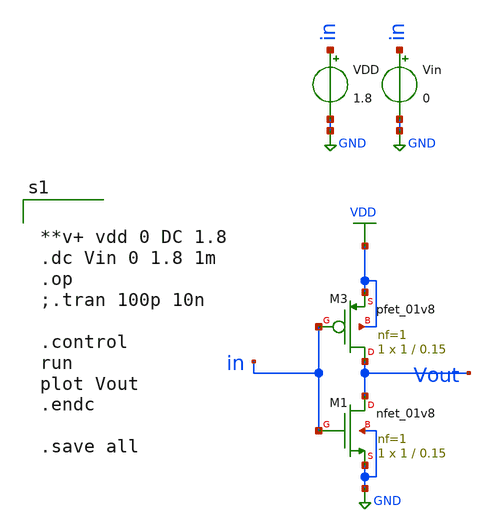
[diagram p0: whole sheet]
** sch_path: inverter.sch
**.subckt inverter
XM3 Vout in VDD VDD sky130_fd_pr__pfet_01v8 L=0.15 W=1 nf=1 ad='int((1 + 1)/2) * 1 / 1 * 0.29' as='int((1 + 2)/2) * 1 / 1 * 0.29'
+ pd='2*int((1 + 1)/2) * (1 / 1 + 0.29)' ps='2*int((1 + 2)/2) * (1 / 1 + 0.29)' nrd='0.29 / 1 ' nrs='0.29 / 1 '
+ sa=0 sb=0 sd=0 mult=1 m=1
Vin in GND 0
XM1 Vout in GND GND sky130_fd_pr__nfet_01v8 L=0.15 W=1 nf=1 ad='int((1 + 1)/2) * 1 / 1 * 0.29' as='int((1 + 2)/2) * 1 / 1 * 0.29'
+ pd='2*int((1 + 1)/2) * (1 / 1 + 0.29)' ps='2*int((1 + 2)/2) * (1 / 1 + 0.29)' nrd='0.29 / 1 ' nrs='0.29 / 1 '
+ sa=0 sb=0 sd=0 mult=1 m=1
VDD in GND 1.8
**** begin user architecture code


**v+ vdd 0 DC 1.8
.dc Vin 0 1.8 1m
.op
;.tran 100p 10n

.control
run
plot Vout
.endc

.save all


**** end user architecture code
**.ends
.GLOBAL GND
.GLOBAL VDD
.end
